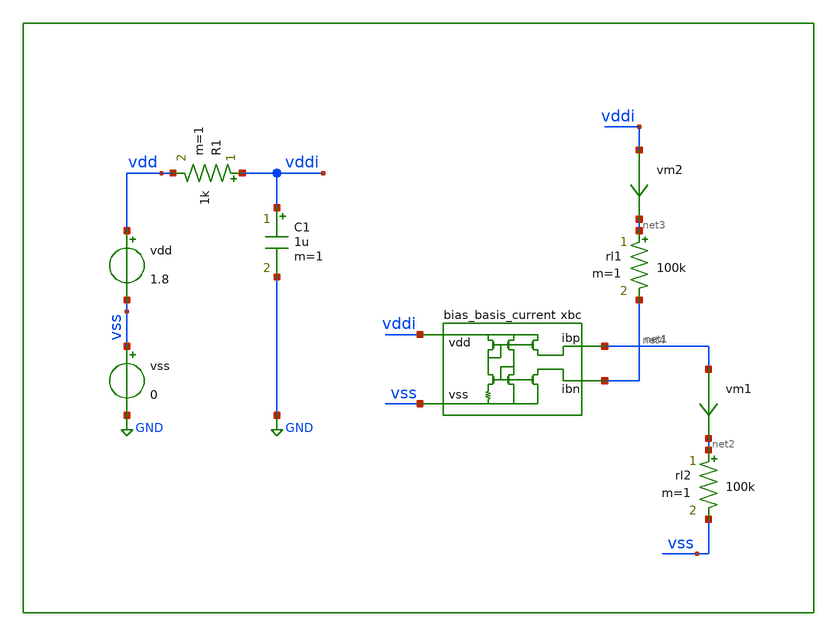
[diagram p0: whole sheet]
** sch_path: xschem/tb/bias/tr_basis_current_startup.sch
**.subckt tr_basis_current_startup
xbc vddi vss net1 net4 bias_basis_current
vm1 net1 net2 0
.save i(vm1)
rl2 net2 vss 100k m=1
vm2 vddi net3 0
.save i(vm2)
rl1 net3 net4 100k m=1
vdd vdd vss 1.8
vss vss GND 0
R1 vddi vdd 1k m=1
C1 vddi GND 1u m=1
**** begin user architecture code

.param MC_SWITCH=0
.temp 27

.control
save all
tran 1u 10m uic
let vm1 = vm1#branch
let vm2 = vm2#branch
plt vm1
plt vm2
.endc



* FET CORNERS
.include $::SKYWATER_MODELS/corners/tt.spice
*.include $::SKYWATER_MODELS/corners/ff.spice
*.include $::SKYWATER_MODELS/corners/ss.spice
*.include $::SKYWATER_MODELS/corners/sf.spice
*.include $::SKYWATER_MODELS/corners/fs.spice

* TT + R + C
*.include $::SKYWATER_MODELS/corners/tt_rmax_cmax.spice
*.include $::SKYWATER_MODELS/corners/tt_rmin_cmin.spice
*.include $::SKYWATER_MODELS/corners/tt_rmax_cmin.spice
*.include $::SKYWATER_MODELS/corners/tt_rmin_cmax.spice

* FF + R + C
*.include $::SKYWATER_MODELS/corners/ff_rmax_cmax.spice
*.include $::SKYWATER_MODELS/corners/ff_rmin_cmin.spice
*.include $::SKYWATER_MODELS/corners/ff_rmax_cmin.spice
*.include $::SKYWATER_MODELS/corners/ff_rmin_cmax.spice


* SS + R + C
*.include $::SKYWATER_MODELS/corners/ss_rmax_cmax.spice
*.include $::SKYWATER_MODELS/corners/ss_rmin_cmin.spice
*.include $::SKYWATER_MODELS/corners/ss_rmax_cmin.spice
*.include $::SKYWATER_MODELS/corners/ss_rmin_cmax.spice

* SF + R + C
*.include $::SKYWATER_MODELS/corners/sf_rmax_cmax.spice
*.include $::SKYWATER_MODELS/corners/sf_rmin_cmin.spice
*.include $::SKYWATER_MODELS/corners/sf_rmax_cmin.spice
*.include $::SKYWATER_MODELS/corners/sf_rmin_cmax.spice

* FS + R + C
*.include $::SKYWATER_MODELS/corners/fs_rmax_cmax.spice
*.include $::SKYWATER_MODELS/corners/fs_rmin_cmin.spice
*.include $::SKYWATER_MODELS/corners/fs_rmax_cmin.spice
*.include $::SKYWATER_MODELS/corners/fs_rmin_cmax.spice

**** end user architecture code
**.ends

* expanding   symbol:  bias/bias_basis_current.sym # of pins=4
** sym_path: xschem/bias/bias_basis_current.sym
** sch_path: xschem/bias/bias_basis_current.sch
.subckt bias_basis_current vdd vss ibp ibn
*.iopin ibn
*.iopin vdd
*.iopin vss
*.iopin ibp
XM5 vbp vbp vdd vdd sky130_fd_pr__pfet_01v8_lvt L=1 W=1 nf=1 ad='int((nf+1)/2) * W/nf * 0.29' as='int((nf+2)/2) * W/nf * 0.29'
+ pd='2*int((nf+1)/2) * (W/nf + 0.29)' ps='2*int((nf+2)/2) * (W/nf + 0.29)' nrd='0.29 / W' nrs='0.29 / W'
+ sa=0 sb=0 sd=0 mult=8 m=8
XM4 vbn vbp vdd vdd sky130_fd_pr__pfet_01v8_lvt L=1 W=1 nf=1 ad='int((nf+1)/2) * W/nf * 0.29' as='int((nf+2)/2) * W/nf * 0.29'
+ pd='2*int((nf+1)/2) * (W/nf + 0.29)' ps='2*int((nf+2)/2) * (W/nf + 0.29)' nrd='0.29 / W' nrs='0.29 / W'
+ sa=0 sb=0 sd=0 mult=8 m=8
XM1 vbn vbn vss vss sky130_fd_pr__nfet_01v8_lvt L=0.5 W=1 nf=1 ad='int((nf+1)/2) * W/nf * 0.29' as='int((nf+2)/2) * W/nf * 0.29'
+ pd='2*int((nf+1)/2) * (W/nf + 0.29)' ps='2*int((nf+2)/2) * (W/nf + 0.29)' nrd='0.29 / W' nrs='0.29 / W'
+ sa=0 sb=0 sd=0 mult=8 m=8
XM2 vbp vbn vres vss sky130_fd_pr__nfet_01v8_lvt L=0.5 W=1 nf=1 ad='int((nf+1)/2) * W/nf * 0.29' as='int((nf+2)/2) * W/nf * 0.29'
+ pd='2*int((nf+1)/2) * (W/nf + 0.29)' ps='2*int((nf+2)/2) * (W/nf + 0.29)' nrd='0.29 / W' nrs='0.29 / W'
+ sa=0 sb=0 sd=0 mult=32 m=32
XM6 ibp vbp vdd vdd sky130_fd_pr__pfet_01v8_lvt L=1 W=1 nf=1 ad='int((nf+1)/2) * W/nf * 0.29' as='int((nf+2)/2) * W/nf * 0.29'
+ pd='2*int((nf+1)/2) * (W/nf + 0.29)' ps='2*int((nf+2)/2) * (W/nf + 0.29)' nrd='0.29 / W' nrs='0.29 / W'
+ sa=0 sb=0 sd=0 mult=2 m=2
XM3 ibn vbn vss vss sky130_fd_pr__nfet_01v8_lvt L=0.5 W=1 nf=1 ad='int((nf+1)/2) * W/nf * 0.29' as='int((nf+2)/2) * W/nf * 0.29'
+ pd='2*int((nf+1)/2) * (W/nf + 0.29)' ps='2*int((nf+2)/2) * (W/nf + 0.29)' nrd='0.29 / W' nrs='0.29 / W'
+ sa=0 sb=0 sd=0 mult=2 m=2
XM7 vsu vsu vss vss sky130_fd_pr__nfet_01v8_lvt L=0.3 W=1 nf=1 ad='int((nf+1)/2) * W/nf * 0.29' as='int((nf+2)/2) * W/nf * 0.29'
+ pd='2*int((nf+1)/2) * (W/nf + 0.29)' ps='2*int((nf+2)/2) * (W/nf + 0.29)' nrd='0.29 / W' nrs='0.29 / W'
+ sa=0 sb=0 sd=0 mult=1 m=1
XM8 vdd vsu vbn vss sky130_fd_pr__nfet_01v8_lvt L=0.3 W=1 nf=1 ad='int((nf+1)/2) * W/nf * 0.29' as='int((nf+2)/2) * W/nf * 0.29'
+ pd='2*int((nf+1)/2) * (W/nf + 0.29)' ps='2*int((nf+2)/2) * (W/nf + 0.29)' nrd='0.29 / W' nrs='0.29 / W'
+ sa=0 sb=0 sd=0 mult=1 m=1
XM9 vsu vsu net1 vdd sky130_fd_pr__pfet_01v8_lvt L=1 W=0.5 nf=1 ad='int((nf+1)/2) * W/nf * 0.29' as='int((nf+2)/2) * W/nf * 0.29'
+ pd='2*int((nf+1)/2) * (W/nf + 0.29)' ps='2*int((nf+2)/2) * (W/nf + 0.29)' nrd='0.29 / W' nrs='0.29 / W'
+ sa=0 sb=0 sd=0 mult=1 m=1
XM10 net1 net1 net2 vdd sky130_fd_pr__pfet_01v8_lvt L=1 W=0.5 nf=1 ad='int((nf+1)/2) * W/nf * 0.29' as='int((nf+2)/2) * W/nf * 0.29'
+ pd='2*int((nf+1)/2) * (W/nf + 0.29)' ps='2*int((nf+2)/2) * (W/nf + 0.29)' nrd='0.29 / W' nrs='0.29 / W'
+ sa=0 sb=0 sd=0 mult=1 m=1
XR2 vss vres vss sky130_fd_pr__res_xhigh_po W=0.35 L=14 mult=1 m=1
XR1 net2 vdd vss sky130_fd_pr__res_xhigh_po W=0.35 L=17 mult=1 m=1
.ends

.GLOBAL GND
.end
